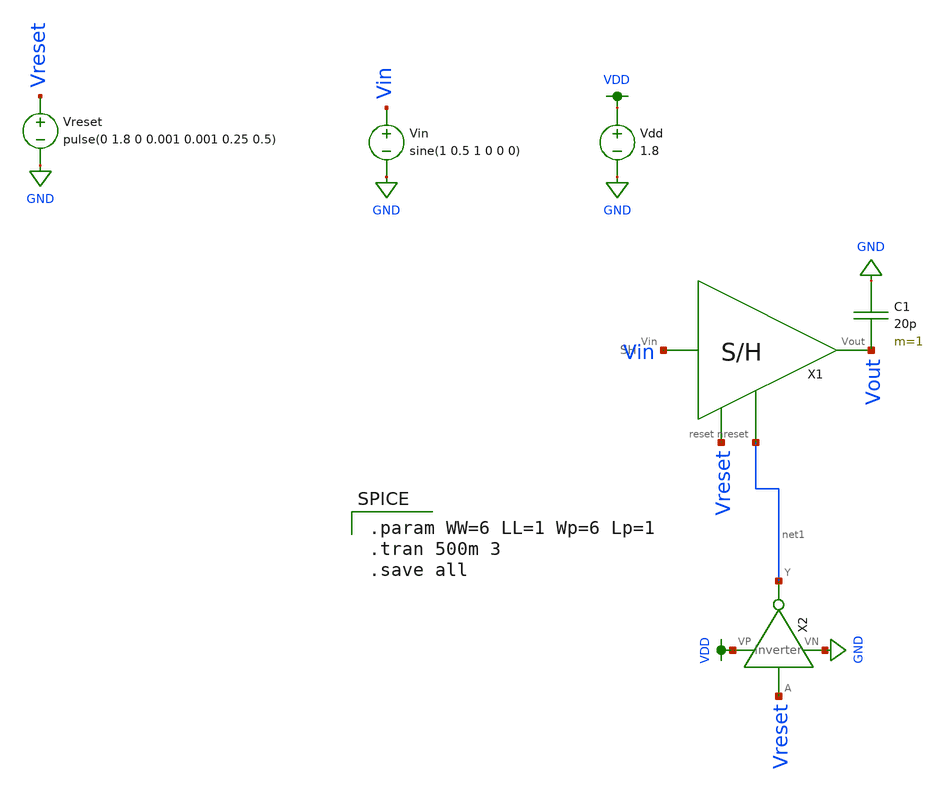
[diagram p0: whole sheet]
** sch_path: schematic/SH_test.sch
**.subckt SH_test
X1 Vreset Vout Vin net1 SH
Vin Vin GND sine(1 0.5 1 0 0 0)
Vdd VDD GND 1.8
Vreset Vreset GND pulse(0 1.8 0 0.001 0.001 0.25 0.5)
X2 Vreset net1 VDD GND inverter
C1 GND Vout 20p m=1
**** begin user architecture code

.option wnflag=1
.param MC_SWITCH=0.0
.lib ~/skywater/skywater-pdk/libraries/sky130_fd_pr_ngspice/latest/models/sky130.lib.spice tt


.param WW=6 LL=1 Wp=6 Lp=1
.tran 500m 3
.save all

**** end user architecture code
**.ends
.GLOBAL GND
.GLOBAL VDD
.end
